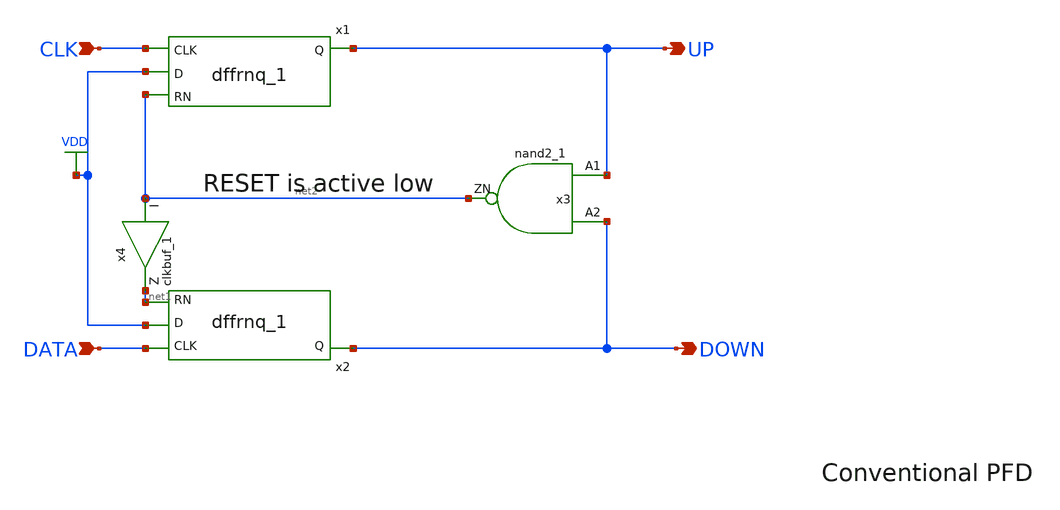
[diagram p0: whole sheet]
** sch_path: PLL/xschem/pfd.sch
**.subckt pfd DATA CLK UP DOWN
*.ipin DATA
*.ipin CLK
*.opin UP
*.opin DOWN
x3 UP DOWN net2 VDD VDD GND GND gf180mcu_fd_sc_mcu7t5v0__nand2_1
x1 VDD net2 CLK UP VDD VDD GND GND gf180mcu_fd_sc_mcu7t5v0__dffrnq_1
x2 VDD net1 DATA DOWN VDD VDD GND GND gf180mcu_fd_sc_mcu7t5v0__dffrnq_1
x4 net2 net1 VDD VDD GND GND gf180mcu_fd_sc_mcu7t5v0__clkbuf_1
**.ends
.GLOBAL VDD
.end
